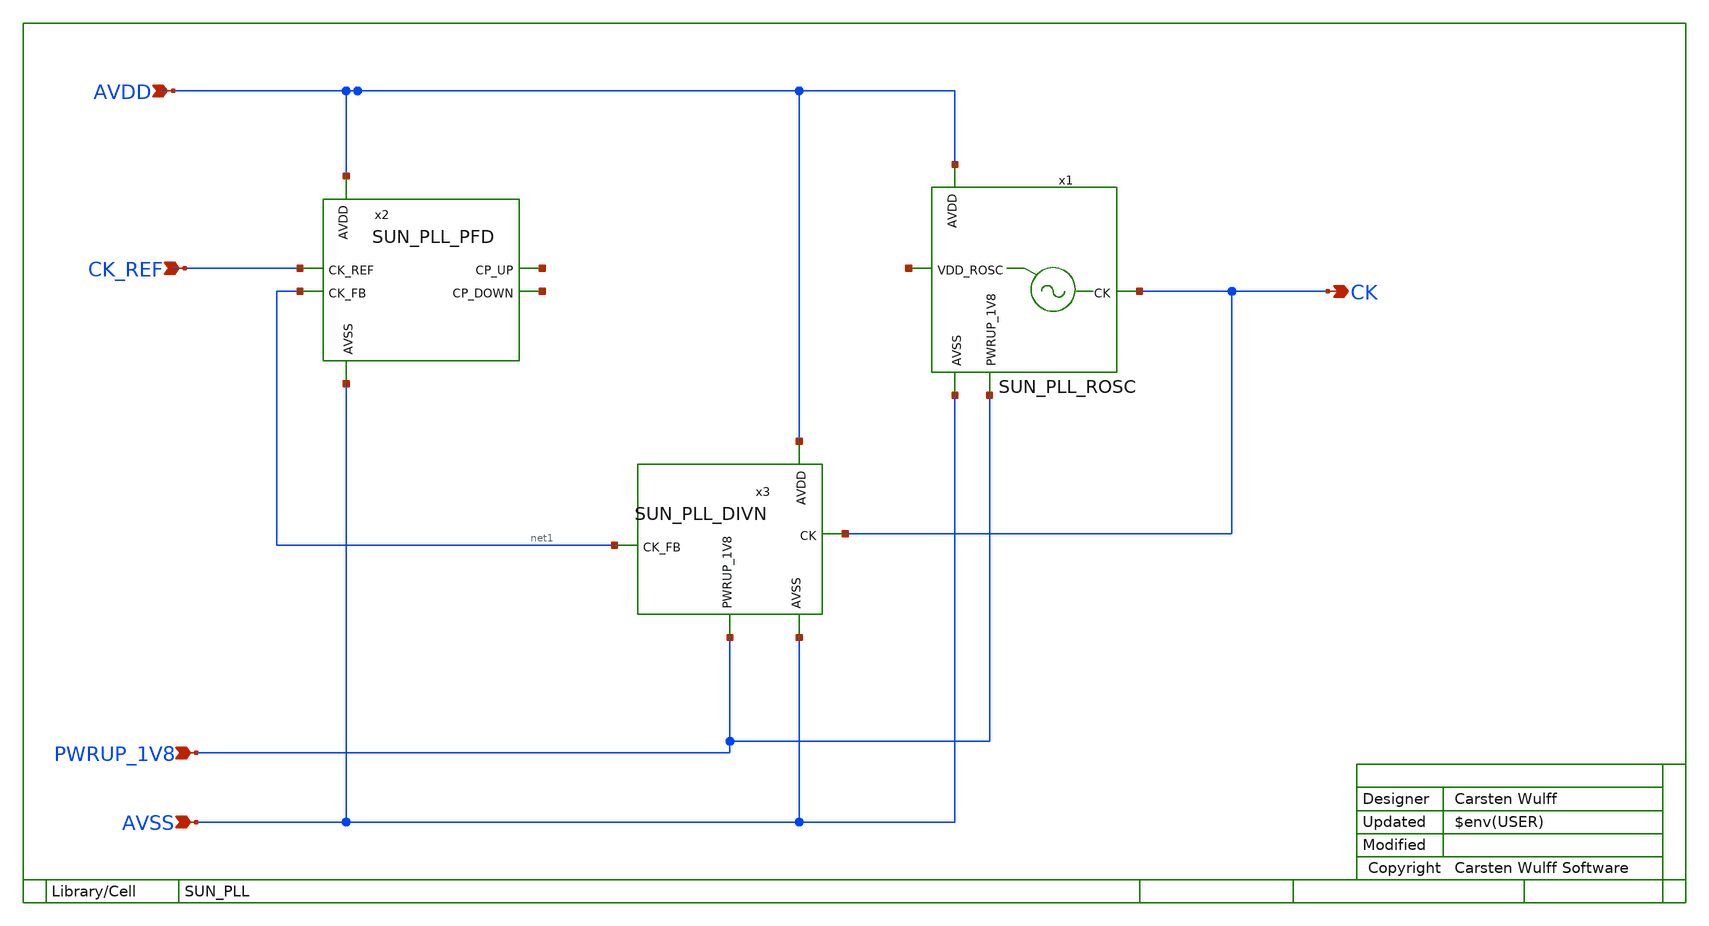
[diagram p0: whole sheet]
** sch_path: ip/sun_pll_sky130nm/design/SUN_PLL_SKY130NM/SUN_PLL.sch
**.subckt SUN_PLL AVDD AVSS PWRUP_1V8 CK_REF CK
*.ipin AVDD
*.ipin AVSS
*.ipin PWRUP_1V8
*.ipin CK_REF
*.opin CK
x1 AVDD CK net2 PWRUP_1V8 AVSS SUN_PLL_ROSC xoffset=0 yoffset=0 angle=0
x2 AVDD net3 CK_REF net4 net1 AVSS SUN_PLL_PFD
x3 AVDD net1 CK PWRUP_1V8 AVSS SUN_PLL_DIVN
**.ends
.end
